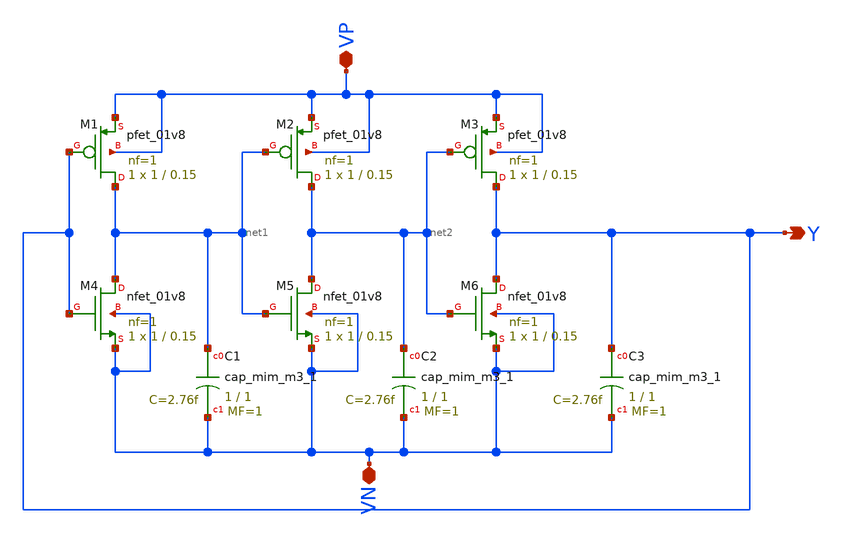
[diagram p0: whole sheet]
** sch_path: Week 3/Week 3/magic_test/xschem/analog.sch
**.subckt analog VP VN Y
*.iopin VP
*.iopin VN
*.opin Y
XM1 net1 Y VP VP sky130_fd_pr__pfet_01v8 L=0.15 W=1 nf=1 ad='int((nf+1)/2) * W/nf * 0.29' as='int((nf+2)/2) * W/nf * 0.29'
+ pd='2*int((nf+1)/2) * (W/nf + 0.29)' ps='2*int((nf+2)/2) * (W/nf + 0.29)' nrd='0.29 / W' nrs='0.29 / W'
+ sa=0 sb=0 sd=0 mult=1 m=1
XM2 net2 net1 VP VP sky130_fd_pr__pfet_01v8 L=0.15 W=1 nf=1 ad='int((nf+1)/2) * W/nf * 0.29' as='int((nf+2)/2) * W/nf * 0.29'
+ pd='2*int((nf+1)/2) * (W/nf + 0.29)' ps='2*int((nf+2)/2) * (W/nf + 0.29)' nrd='0.29 / W' nrs='0.29 / W'
+ sa=0 sb=0 sd=0 mult=1 m=1
XM3 Y net2 VP VP sky130_fd_pr__pfet_01v8 L=0.15 W=1 nf=1 ad='int((nf+1)/2) * W/nf * 0.29' as='int((nf+2)/2) * W/nf * 0.29'
+ pd='2*int((nf+1)/2) * (W/nf + 0.29)' ps='2*int((nf+2)/2) * (W/nf + 0.29)' nrd='0.29 / W' nrs='0.29 / W'
+ sa=0 sb=0 sd=0 mult=1 m=1
XM4 net1 Y VN VN sky130_fd_pr__nfet_01v8 L=0.15 W=1 nf=1 ad='int((nf+1)/2) * W/nf * 0.29' as='int((nf+2)/2) * W/nf * 0.29'
+ pd='2*int((nf+1)/2) * (W/nf + 0.29)' ps='2*int((nf+2)/2) * (W/nf + 0.29)' nrd='0.29 / W' nrs='0.29 / W'
+ sa=0 sb=0 sd=0 mult=1 m=1
XM5 net2 net1 VN VN sky130_fd_pr__nfet_01v8 L=0.15 W=1 nf=1 ad='int((nf+1)/2) * W/nf * 0.29' as='int((nf+2)/2) * W/nf * 0.29'
+ pd='2*int((nf+1)/2) * (W/nf + 0.29)' ps='2*int((nf+2)/2) * (W/nf + 0.29)' nrd='0.29 / W' nrs='0.29 / W'
+ sa=0 sb=0 sd=0 mult=1 m=1
XM6 Y net2 VN VN sky130_fd_pr__nfet_01v8 L=0.15 W=1 nf=1 ad='int((nf+1)/2) * W/nf * 0.29' as='int((nf+2)/2) * W/nf * 0.29'
+ pd='2*int((nf+1)/2) * (W/nf + 0.29)' ps='2*int((nf+2)/2) * (W/nf + 0.29)' nrd='0.29 / W' nrs='0.29 / W'
+ sa=0 sb=0 sd=0 mult=1 m=1
XC1 net1 VN sky130_fd_pr__cap_mim_m3_1 W=1 L=1 MF=1 m=1
XC2 net2 VN sky130_fd_pr__cap_mim_m3_1 W=1 L=1 MF=1 m=1
XC3 Y VN sky130_fd_pr__cap_mim_m3_1 W=1 L=1 MF=1 m=1
**.ends
.end
